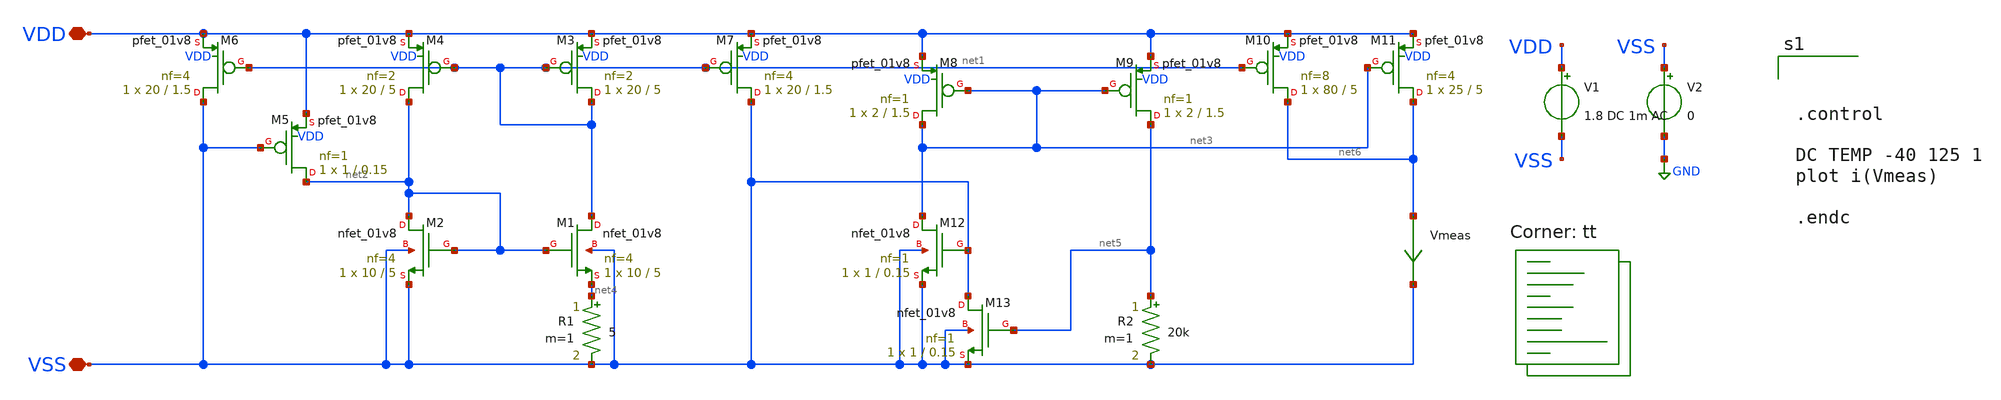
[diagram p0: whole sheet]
** sch_path: bandgap/current-mode-bgr/current-mode-bgr.sch
**.subckt current-mode-bgr VDD VSS
*.iopin VDD
*.iopin VSS
XM1 net1 net2 net4 VSS sky130_fd_pr__nfet_01v8 L=5 W=10 nf=4 ad='int((nf+1)/2) * W/nf * 0.29' as='int((nf+2)/2) * W/nf * 0.29'
+ pd='2*int((nf+1)/2) * (W/nf + 0.29)' ps='2*int((nf+2)/2) * (W/nf + 0.29)' nrd='0.29 / W' nrs='0.29 / W'
+ sa=0 sb=0 sd=0 mult=1 m=1
XM2 net2 net2 VSS VSS sky130_fd_pr__nfet_01v8 L=5 W=10 nf=4 ad='int((nf+1)/2) * W/nf * 0.29' as='int((nf+2)/2) * W/nf * 0.29'
+ pd='2*int((nf+1)/2) * (W/nf + 0.29)' ps='2*int((nf+2)/2) * (W/nf + 0.29)' nrd='0.29 / W' nrs='0.29 / W'
+ sa=0 sb=0 sd=0 mult=1 m=1
XM3 net1 net1 VDD VDD sky130_fd_pr__pfet_01v8 L=5 W=20 nf=2 ad='int((nf+1)/2) * W/nf * 0.29' as='int((nf+2)/2) * W/nf * 0.29'
+ pd='2*int((nf+1)/2) * (W/nf + 0.29)' ps='2*int((nf+2)/2) * (W/nf + 0.29)' nrd='0.29 / W' nrs='0.29 / W'
+ sa=0 sb=0 sd=0 mult=1 m=1
XM4 net2 net1 VDD VDD sky130_fd_pr__pfet_01v8 L=5 W=20 nf=2 ad='int((nf+1)/2) * W/nf * 0.29' as='int((nf+2)/2) * W/nf * 0.29'
+ pd='2*int((nf+1)/2) * (W/nf + 0.29)' ps='2*int((nf+2)/2) * (W/nf + 0.29)' nrd='0.29 / W' nrs='0.29 / W'
+ sa=0 sb=0 sd=0 mult=1 m=1
XM5 net2 VSS VDD VDD sky130_fd_pr__pfet_01v8 L=0.15 W=1 nf=1 ad='int((nf+1)/2) * W/nf * 0.29' as='int((nf+2)/2) * W/nf * 0.29'
+ pd='2*int((nf+1)/2) * (W/nf + 0.29)' ps='2*int((nf+2)/2) * (W/nf + 0.29)' nrd='0.29 / W' nrs='0.29 / W'
+ sa=0 sb=0 sd=0 mult=1 m=1
XM6 VSS net1 VDD VDD sky130_fd_pr__pfet_01v8 L=1.5 W=20 nf=4 ad='int((nf+1)/2) * W/nf * 0.29' as='int((nf+2)/2) * W/nf * 0.29'
+ pd='2*int((nf+1)/2) * (W/nf + 0.29)' ps='2*int((nf+2)/2) * (W/nf + 0.29)' nrd='0.29 / W' nrs='0.29 / W'
+ sa=0 sb=0 sd=0 mult=1 m=1
XM7 VSS net1 VDD VDD sky130_fd_pr__pfet_01v8 L=1.5 W=20 nf=4 ad='int((nf+1)/2) * W/nf * 0.29' as='int((nf+2)/2) * W/nf * 0.29'
+ pd='2*int((nf+1)/2) * (W/nf + 0.29)' ps='2*int((nf+2)/2) * (W/nf + 0.29)' nrd='0.29 / W' nrs='0.29 / W'
+ sa=0 sb=0 sd=0 mult=1 m=1
XM8 net3 net3 VDD VDD sky130_fd_pr__pfet_01v8 L=1.5 W=2 nf=1 ad='int((nf+1)/2) * W/nf * 0.29' as='int((nf+2)/2) * W/nf * 0.29'
+ pd='2*int((nf+1)/2) * (W/nf + 0.29)' ps='2*int((nf+2)/2) * (W/nf + 0.29)' nrd='0.29 / W' nrs='0.29 / W'
+ sa=0 sb=0 sd=0 mult=1 m=1
XM9 net5 net3 VDD VDD sky130_fd_pr__pfet_01v8 L=1.5 W=2 nf=1 ad='int((nf+1)/2) * W/nf * 0.29' as='int((nf+2)/2) * W/nf * 0.29'
+ pd='2*int((nf+1)/2) * (W/nf + 0.29)' ps='2*int((nf+2)/2) * (W/nf + 0.29)' nrd='0.29 / W' nrs='0.29 / W'
+ sa=0 sb=0 sd=0 mult=1 m=1
XM10 net6 net1 VDD VDD sky130_fd_pr__pfet_01v8 L=5 W=80 nf=8 ad='int((nf+1)/2) * W/nf * 0.29' as='int((nf+2)/2) * W/nf * 0.29'
+ pd='2*int((nf+1)/2) * (W/nf + 0.29)' ps='2*int((nf+2)/2) * (W/nf + 0.29)' nrd='0.29 / W' nrs='0.29 / W'
+ sa=0 sb=0 sd=0 mult=1 m=1
XM11 net6 net3 VDD VDD sky130_fd_pr__pfet_01v8 L=5 W=25 nf=4 ad='int((nf+1)/2) * W/nf * 0.29' as='int((nf+2)/2) * W/nf * 0.29'
+ pd='2*int((nf+1)/2) * (W/nf + 0.29)' ps='2*int((nf+2)/2) * (W/nf + 0.29)' nrd='0.29 / W' nrs='0.29 / W'
+ sa=0 sb=0 sd=0 mult=1 m=1
XM12 net3 VSS VSS VSS sky130_fd_pr__nfet_01v8 L=0.15 W=1 nf=1 ad='int((nf+1)/2) * W/nf * 0.29' as='int((nf+2)/2) * W/nf * 0.29'
+ pd='2*int((nf+1)/2) * (W/nf + 0.29)' ps='2*int((nf+2)/2) * (W/nf + 0.29)' nrd='0.29 / W' nrs='0.29 / W'
+ sa=0 sb=0 sd=0 mult=1 m=1
XM13 VSS net5 VSS VSS sky130_fd_pr__nfet_01v8 L=0.15 W=1 nf=1 ad='int((nf+1)/2) * W/nf * 0.29' as='int((nf+2)/2) * W/nf * 0.29'
+ pd='2*int((nf+1)/2) * (W/nf + 0.29)' ps='2*int((nf+2)/2) * (W/nf + 0.29)' nrd='0.29 / W' nrs='0.29 / W'
+ sa=0 sb=0 sd=0 mult=1 m=1
R1 net4 VSS 5 m=1
R2 net5 VSS 20k m=1
V1 VDD VSS 1.8 DC 1m AC
V2 VSS GND 0
Vmeas net6 VSS 0
.save i(vmeas)
**** begin user architecture code
.lib $::SKYWATER_MODELS/sky130.lib.spice tt



.control

DC TEMP -40 125 1
plot i(Vmeas)

.endc


**** end user architecture code
**.ends
.GLOBAL GND
.end
